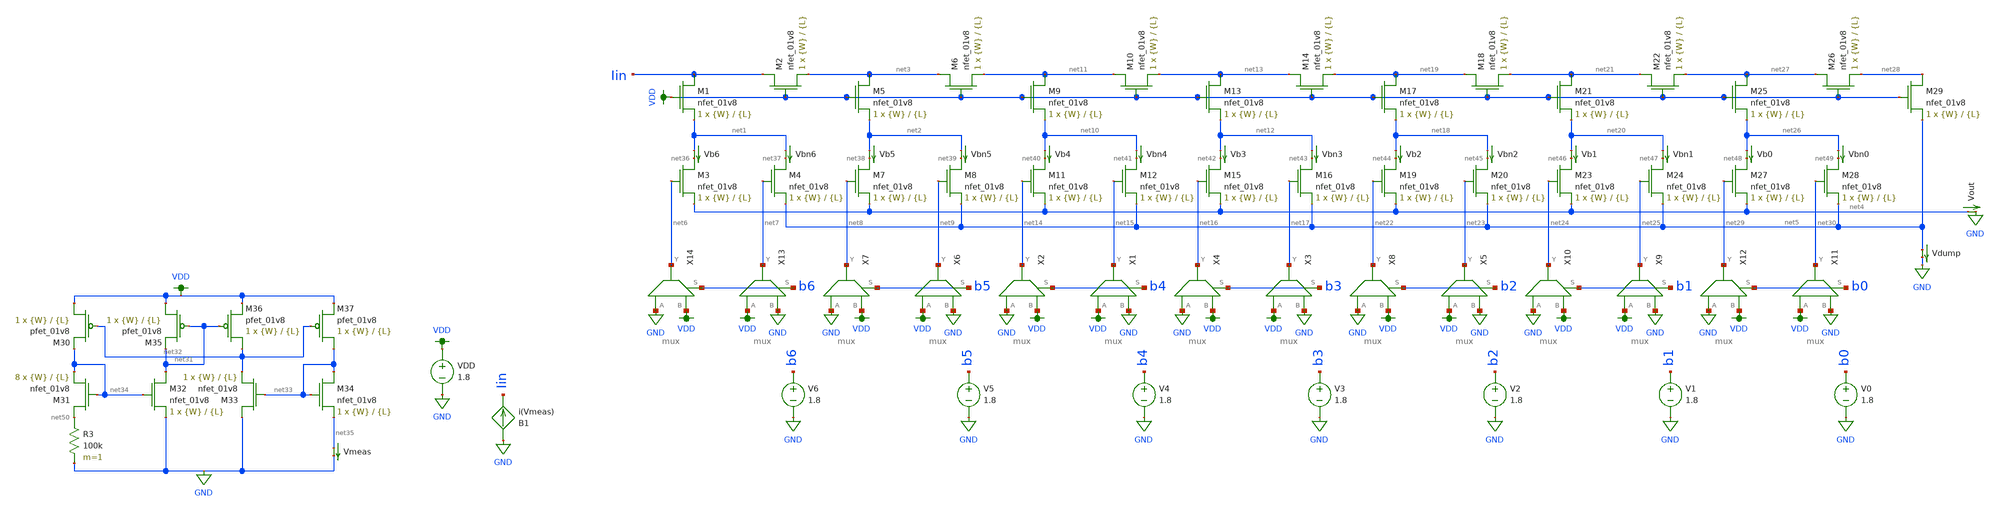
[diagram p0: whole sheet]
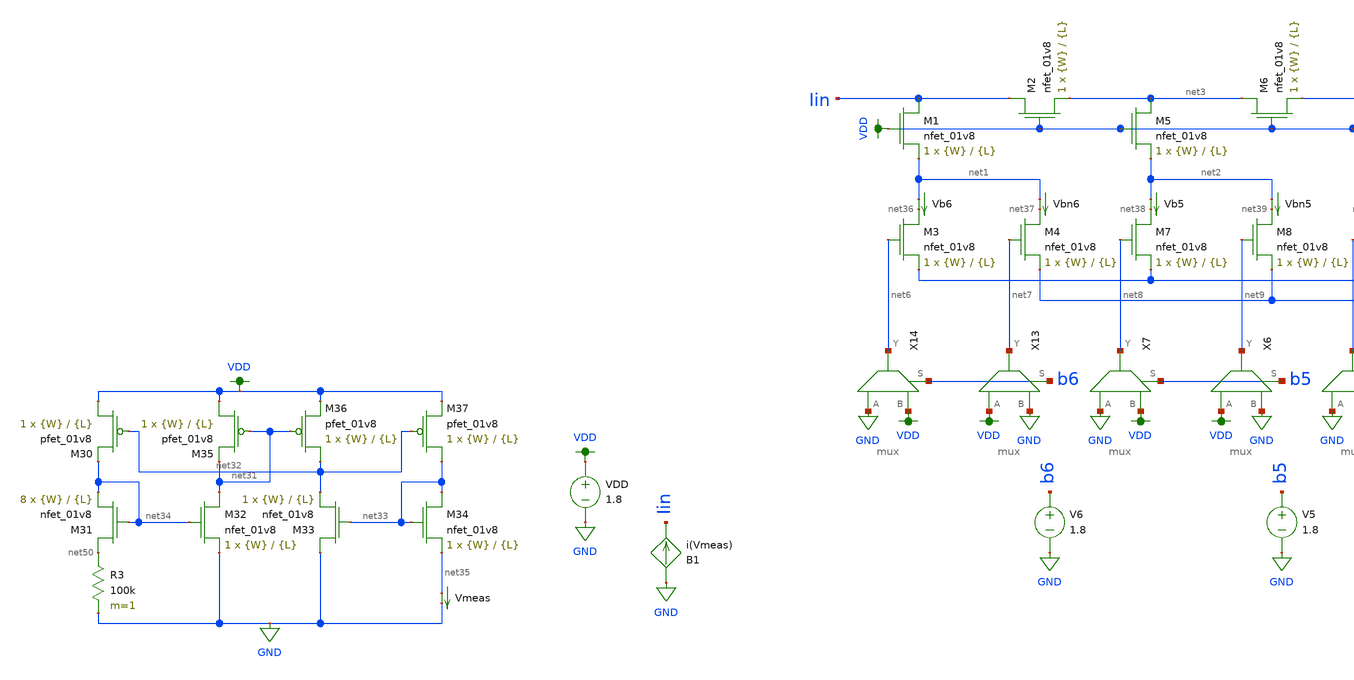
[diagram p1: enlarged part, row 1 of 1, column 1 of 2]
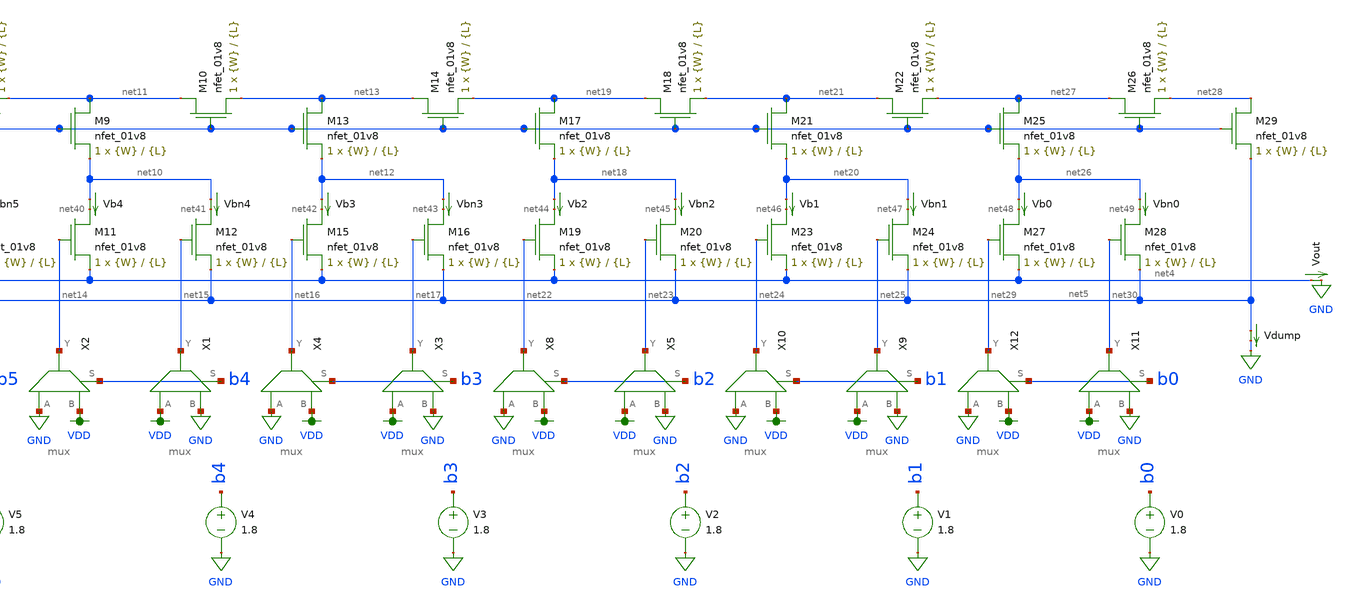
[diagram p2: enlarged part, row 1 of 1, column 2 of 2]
** sch_path: schematics/dac_from_paper.sch
**.subckt dac_from_paper
XM1 Iin VDD net1 GND sky130_fd_pr__nfet_01v8 L={L} W={W} nf=1 ad='int((nf+1)/2) * W/nf * 0.29' as='int((nf+2)/2) * W/nf * 0.29'
+ pd='2*int((nf+1)/2) * (W/nf + 0.29)' ps='2*int((nf+2)/2) * (W/nf + 0.29)' nrd='0.29 / W' nrs='0.29 / W'
+ sa=0 sb=0 sd=0 mult=1 m=1
XM2 Iin VDD net3 GND sky130_fd_pr__nfet_01v8 L={L} W={W} nf=1 ad='int((nf+1)/2) * W/nf * 0.29' as='int((nf+2)/2) * W/nf * 0.29'
+ pd='2*int((nf+1)/2) * (W/nf + 0.29)' ps='2*int((nf+2)/2) * (W/nf + 0.29)' nrd='0.29 / W' nrs='0.29 / W'
+ sa=0 sb=0 sd=0 mult=1 m=1
XM3 net36 net6 net4 GND sky130_fd_pr__nfet_01v8 L={L} W={W} nf=1 ad='int((nf+1)/2) * W/nf * 0.29' as='int((nf+2)/2) * W/nf * 0.29'
+ pd='2*int((nf+1)/2) * (W/nf + 0.29)' ps='2*int((nf+2)/2) * (W/nf + 0.29)' nrd='0.29 / W' nrs='0.29 / W'
+ sa=0 sb=0 sd=0 mult=1 m=1
XM4 net37 net7 net5 GND sky130_fd_pr__nfet_01v8 L={L} W={W} nf=1 ad='int((nf+1)/2) * W/nf * 0.29' as='int((nf+2)/2) * W/nf * 0.29'
+ pd='2*int((nf+1)/2) * (W/nf + 0.29)' ps='2*int((nf+2)/2) * (W/nf + 0.29)' nrd='0.29 / W' nrs='0.29 / W'
+ sa=0 sb=0 sd=0 mult=1 m=1
XM5 net3 VDD net2 GND sky130_fd_pr__nfet_01v8 L={L} W={W} nf=1 ad='int((nf+1)/2) * W/nf * 0.29' as='int((nf+2)/2) * W/nf * 0.29'
+ pd='2*int((nf+1)/2) * (W/nf + 0.29)' ps='2*int((nf+2)/2) * (W/nf + 0.29)' nrd='0.29 / W' nrs='0.29 / W'
+ sa=0 sb=0 sd=0 mult=1 m=1
XM6 net3 VDD net11 GND sky130_fd_pr__nfet_01v8 L={L} W={W} nf=1 ad='int((nf+1)/2) * W/nf * 0.29' as='int((nf+2)/2) * W/nf * 0.29'
+ pd='2*int((nf+1)/2) * (W/nf + 0.29)' ps='2*int((nf+2)/2) * (W/nf + 0.29)' nrd='0.29 / W' nrs='0.29 / W'
+ sa=0 sb=0 sd=0 mult=1 m=1
XM7 net38 net8 net4 GND sky130_fd_pr__nfet_01v8 L={L} W={W} nf=1 ad='int((nf+1)/2) * W/nf * 0.29' as='int((nf+2)/2) * W/nf * 0.29'
+ pd='2*int((nf+1)/2) * (W/nf + 0.29)' ps='2*int((nf+2)/2) * (W/nf + 0.29)' nrd='0.29 / W' nrs='0.29 / W'
+ sa=0 sb=0 sd=0 mult=1 m=1
XM8 net39 net9 net5 GND sky130_fd_pr__nfet_01v8 L={L} W={W} nf=1 ad='int((nf+1)/2) * W/nf * 0.29' as='int((nf+2)/2) * W/nf * 0.29'
+ pd='2*int((nf+1)/2) * (W/nf + 0.29)' ps='2*int((nf+2)/2) * (W/nf + 0.29)' nrd='0.29 / W' nrs='0.29 / W'
+ sa=0 sb=0 sd=0 mult=1 m=1
XM9 net11 VDD net10 GND sky130_fd_pr__nfet_01v8 L={L} W={W} nf=1 ad='int((nf+1)/2) * W/nf * 0.29' as='int((nf+2)/2) * W/nf * 0.29'
+ pd='2*int((nf+1)/2) * (W/nf + 0.29)' ps='2*int((nf+2)/2) * (W/nf + 0.29)' nrd='0.29 / W' nrs='0.29 / W'
+ sa=0 sb=0 sd=0 mult=1 m=1
XM10 net11 VDD net13 GND sky130_fd_pr__nfet_01v8 L={L} W={W} nf=1 ad='int((nf+1)/2) * W/nf * 0.29' as='int((nf+2)/2) * W/nf * 0.29'
+ pd='2*int((nf+1)/2) * (W/nf + 0.29)' ps='2*int((nf+2)/2) * (W/nf + 0.29)' nrd='0.29 / W' nrs='0.29 / W'
+ sa=0 sb=0 sd=0 mult=1 m=1
XM11 net40 net14 net4 GND sky130_fd_pr__nfet_01v8 L={L} W={W} nf=1 ad='int((nf+1)/2) * W/nf * 0.29' as='int((nf+2)/2) * W/nf * 0.29'
+ pd='2*int((nf+1)/2) * (W/nf + 0.29)' ps='2*int((nf+2)/2) * (W/nf + 0.29)' nrd='0.29 / W' nrs='0.29 / W'
+ sa=0 sb=0 sd=0 mult=1 m=1
XM12 net41 net15 net5 GND sky130_fd_pr__nfet_01v8 L={L} W={W} nf=1 ad='int((nf+1)/2) * W/nf * 0.29' as='int((nf+2)/2) * W/nf * 0.29'
+ pd='2*int((nf+1)/2) * (W/nf + 0.29)' ps='2*int((nf+2)/2) * (W/nf + 0.29)' nrd='0.29 / W' nrs='0.29 / W'
+ sa=0 sb=0 sd=0 mult=1 m=1
XM13 net13 VDD net12 GND sky130_fd_pr__nfet_01v8 L={L} W={W} nf=1 ad='int((nf+1)/2) * W/nf * 0.29' as='int((nf+2)/2) * W/nf * 0.29'
+ pd='2*int((nf+1)/2) * (W/nf + 0.29)' ps='2*int((nf+2)/2) * (W/nf + 0.29)' nrd='0.29 / W' nrs='0.29 / W'
+ sa=0 sb=0 sd=0 mult=1 m=1
XM14 net13 VDD net19 GND sky130_fd_pr__nfet_01v8 L={L} W={W} nf=1 ad='int((nf+1)/2) * W/nf * 0.29' as='int((nf+2)/2) * W/nf * 0.29'
+ pd='2*int((nf+1)/2) * (W/nf + 0.29)' ps='2*int((nf+2)/2) * (W/nf + 0.29)' nrd='0.29 / W' nrs='0.29 / W'
+ sa=0 sb=0 sd=0 mult=1 m=1
XM15 net42 net16 net4 GND sky130_fd_pr__nfet_01v8 L={L} W={W} nf=1 ad='int((nf+1)/2) * W/nf * 0.29' as='int((nf+2)/2) * W/nf * 0.29'
+ pd='2*int((nf+1)/2) * (W/nf + 0.29)' ps='2*int((nf+2)/2) * (W/nf + 0.29)' nrd='0.29 / W' nrs='0.29 / W'
+ sa=0 sb=0 sd=0 mult=1 m=1
XM16 net43 net17 net5 GND sky130_fd_pr__nfet_01v8 L={L} W={W} nf=1 ad='int((nf+1)/2) * W/nf * 0.29' as='int((nf+2)/2) * W/nf * 0.29'
+ pd='2*int((nf+1)/2) * (W/nf + 0.29)' ps='2*int((nf+2)/2) * (W/nf + 0.29)' nrd='0.29 / W' nrs='0.29 / W'
+ sa=0 sb=0 sd=0 mult=1 m=1
XM17 net19 VDD net18 GND sky130_fd_pr__nfet_01v8 L={L} W={W} nf=1 ad='int((nf+1)/2) * W/nf * 0.29' as='int((nf+2)/2) * W/nf * 0.29'
+ pd='2*int((nf+1)/2) * (W/nf + 0.29)' ps='2*int((nf+2)/2) * (W/nf + 0.29)' nrd='0.29 / W' nrs='0.29 / W'
+ sa=0 sb=0 sd=0 mult=1 m=1
XM18 net19 VDD net21 GND sky130_fd_pr__nfet_01v8 L={L} W={W} nf=1 ad='int((nf+1)/2) * W/nf * 0.29' as='int((nf+2)/2) * W/nf * 0.29'
+ pd='2*int((nf+1)/2) * (W/nf + 0.29)' ps='2*int((nf+2)/2) * (W/nf + 0.29)' nrd='0.29 / W' nrs='0.29 / W'
+ sa=0 sb=0 sd=0 mult=1 m=1
XM19 net44 net22 net4 GND sky130_fd_pr__nfet_01v8 L={L} W={W} nf=1 ad='int((nf+1)/2) * W/nf * 0.29' as='int((nf+2)/2) * W/nf * 0.29'
+ pd='2*int((nf+1)/2) * (W/nf + 0.29)' ps='2*int((nf+2)/2) * (W/nf + 0.29)' nrd='0.29 / W' nrs='0.29 / W'
+ sa=0 sb=0 sd=0 mult=1 m=1
XM20 net45 net23 net5 GND sky130_fd_pr__nfet_01v8 L={L} W={W} nf=1 ad='int((nf+1)/2) * W/nf * 0.29' as='int((nf+2)/2) * W/nf * 0.29'
+ pd='2*int((nf+1)/2) * (W/nf + 0.29)' ps='2*int((nf+2)/2) * (W/nf + 0.29)' nrd='0.29 / W' nrs='0.29 / W'
+ sa=0 sb=0 sd=0 mult=1 m=1
XM21 net21 VDD net20 GND sky130_fd_pr__nfet_01v8 L={L} W={W} nf=1 ad='int((nf+1)/2) * W/nf * 0.29' as='int((nf+2)/2) * W/nf * 0.29'
+ pd='2*int((nf+1)/2) * (W/nf + 0.29)' ps='2*int((nf+2)/2) * (W/nf + 0.29)' nrd='0.29 / W' nrs='0.29 / W'
+ sa=0 sb=0 sd=0 mult=1 m=1
XM22 net21 VDD net27 GND sky130_fd_pr__nfet_01v8 L={L} W={W} nf=1 ad='int((nf+1)/2) * W/nf * 0.29' as='int((nf+2)/2) * W/nf * 0.29'
+ pd='2*int((nf+1)/2) * (W/nf + 0.29)' ps='2*int((nf+2)/2) * (W/nf + 0.29)' nrd='0.29 / W' nrs='0.29 / W'
+ sa=0 sb=0 sd=0 mult=1 m=1
XM23 net46 net24 net4 GND sky130_fd_pr__nfet_01v8 L={L} W={W} nf=1 ad='int((nf+1)/2) * W/nf * 0.29' as='int((nf+2)/2) * W/nf * 0.29'
+ pd='2*int((nf+1)/2) * (W/nf + 0.29)' ps='2*int((nf+2)/2) * (W/nf + 0.29)' nrd='0.29 / W' nrs='0.29 / W'
+ sa=0 sb=0 sd=0 mult=1 m=1
XM24 net47 net25 net5 GND sky130_fd_pr__nfet_01v8 L={L} W={W} nf=1 ad='int((nf+1)/2) * W/nf * 0.29' as='int((nf+2)/2) * W/nf * 0.29'
+ pd='2*int((nf+1)/2) * (W/nf + 0.29)' ps='2*int((nf+2)/2) * (W/nf + 0.29)' nrd='0.29 / W' nrs='0.29 / W'
+ sa=0 sb=0 sd=0 mult=1 m=1
XM25 net27 VDD net26 GND sky130_fd_pr__nfet_01v8 L={L} W={W} nf=1 ad='int((nf+1)/2) * W/nf * 0.29' as='int((nf+2)/2) * W/nf * 0.29'
+ pd='2*int((nf+1)/2) * (W/nf + 0.29)' ps='2*int((nf+2)/2) * (W/nf + 0.29)' nrd='0.29 / W' nrs='0.29 / W'
+ sa=0 sb=0 sd=0 mult=1 m=1
XM26 net27 VDD net28 GND sky130_fd_pr__nfet_01v8 L={L} W={W} nf=1 ad='int((nf+1)/2) * W/nf * 0.29' as='int((nf+2)/2) * W/nf * 0.29'
+ pd='2*int((nf+1)/2) * (W/nf + 0.29)' ps='2*int((nf+2)/2) * (W/nf + 0.29)' nrd='0.29 / W' nrs='0.29 / W'
+ sa=0 sb=0 sd=0 mult=1 m=1
XM27 net48 net29 net4 GND sky130_fd_pr__nfet_01v8 L={L} W={W} nf=1 ad='int((nf+1)/2) * W/nf * 0.29' as='int((nf+2)/2) * W/nf * 0.29'
+ pd='2*int((nf+1)/2) * (W/nf + 0.29)' ps='2*int((nf+2)/2) * (W/nf + 0.29)' nrd='0.29 / W' nrs='0.29 / W'
+ sa=0 sb=0 sd=0 mult=1 m=1
XM28 net49 net30 net5 GND sky130_fd_pr__nfet_01v8 L={L} W={W} nf=1 ad='int((nf+1)/2) * W/nf * 0.29' as='int((nf+2)/2) * W/nf * 0.29'
+ pd='2*int((nf+1)/2) * (W/nf + 0.29)' ps='2*int((nf+2)/2) * (W/nf + 0.29)' nrd='0.29 / W' nrs='0.29 / W'
+ sa=0 sb=0 sd=0 mult=1 m=1
XM29 net28 VDD net5 GND sky130_fd_pr__nfet_01v8 L={L} W={W} nf=1 ad='int((nf+1)/2) * W/nf * 0.29' as='int((nf+2)/2) * W/nf * 0.29'
+ pd='2*int((nf+1)/2) * (W/nf + 0.29)' ps='2*int((nf+2)/2) * (W/nf + 0.29)' nrd='0.29 / W' nrs='0.29 / W'
+ sa=0 sb=0 sd=0 mult=1 m=1
Vdump net5 GND 0
.save i(vdump)
Vb0 net26 net48 0
.save i(vb0)
Vbn0 net26 net49 0
.save i(vbn0)
Vb5 net2 net38 0
.save i(vb5)
Vb6 net1 net36 0
.save i(vb6)
Vout net4 GND 0
.save i(vout)
Vb1 net20 net46 0
.save i(vb1)
Vb2 net18 net44 0
.save i(vb2)
Vb3 net12 net42 0
.save i(vb3)
Vb4 net10 net40 0
.save i(vb4)
Vbn1 net20 net47 0
.save i(vbn1)
Vbn2 net18 net45 0
.save i(vbn2)
Vbn3 net12 net43 0
.save i(vbn3)
Vbn4 net10 net41 0
.save i(vbn4)
Vbn5 net2 net39 0
.save i(vbn5)
Vbn6 net1 net37 0
.save i(vbn6)
V0 b0 GND 1.8
V1 b1 GND 1.8
V2 b2 GND 1.8
V3 b3 GND 1.8
V4 b4 GND 1.8
V5 b5 GND 1.8
V6 b6 GND 1.8
XM30 VDD net32 net34 VDD sky130_fd_pr__pfet_01v8 L={L} W={W} nf=1 ad='int((nf+1)/2) * W/nf * 0.29' as='int((nf+2)/2) * W/nf * 0.29'
+ pd='2*int((nf+1)/2) * (W/nf + 0.29)' ps='2*int((nf+2)/2) * (W/nf + 0.29)' nrd='0.29 / W' nrs='0.29 / W'
+ sa=0 sb=0 sd=0 mult=1 m=1
XM31 net50 net34 net34 GND sky130_fd_pr__nfet_01v8 L={L} W={W} nf=1 ad='int((nf+1)/2) * W/nf * 0.29'
+ as='int((nf+2)/2) * W/nf * 0.29' pd='2*int((nf+1)/2) * (W/nf + 0.29)' ps='2*int((nf+2)/2) * (W/nf + 0.29)'
+ nrd='0.29 / W' nrs='0.29 / W' sa=0 sb=0 sd=0 mult=8 m=8
R3 net50 GND 100k m=1
XM32 net31 net34 GND GND sky130_fd_pr__nfet_01v8 L={L} W={W} nf=1 ad='int((nf+1)/2) * W/nf * 0.29' as='int((nf+2)/2) * W/nf * 0.29'
+ pd='2*int((nf+1)/2) * (W/nf + 0.29)' ps='2*int((nf+2)/2) * (W/nf + 0.29)' nrd='0.29 / W' nrs='0.29 / W'
+ sa=0 sb=0 sd=0 mult=1 m=1
XM33 GND net33 net32 GND sky130_fd_pr__nfet_01v8 L={L} W={W} nf=1 ad='int((nf+1)/2) * W/nf * 0.29' as='int((nf+2)/2) * W/nf * 0.29'
+ pd='2*int((nf+1)/2) * (W/nf + 0.29)' ps='2*int((nf+2)/2) * (W/nf + 0.29)' nrd='0.29 / W' nrs='0.29 / W'
+ sa=0 sb=0 sd=0 mult=1 m=1
XM34 net33 net33 net35 GND sky130_fd_pr__nfet_01v8 L={L} W={W} nf=1 ad='int((nf+1)/2) * W/nf * 0.29'
+ as='int((nf+2)/2) * W/nf * 0.29' pd='2*int((nf+1)/2) * (W/nf + 0.29)' ps='2*int((nf+2)/2) * (W/nf + 0.29)'
+ nrd='0.29 / W' nrs='0.29 / W' sa=0 sb=0 sd=0 mult=1 m=1
XM35 VDD net31 net31 VDD sky130_fd_pr__pfet_01v8 L={L} W={W} nf=1 ad='int((nf+1)/2) * W/nf * 0.29' as='int((nf+2)/2) * W/nf * 0.29'
+ pd='2*int((nf+1)/2) * (W/nf + 0.29)' ps='2*int((nf+2)/2) * (W/nf + 0.29)' nrd='0.29 / W' nrs='0.29 / W'
+ sa=0 sb=0 sd=0 mult=1 m=1
XM36 net32 net31 VDD VDD sky130_fd_pr__pfet_01v8 L={L} W={W} nf=1 ad='int((nf+1)/2) * W/nf * 0.29' as='int((nf+2)/2) * W/nf * 0.29'
+ pd='2*int((nf+1)/2) * (W/nf + 0.29)' ps='2*int((nf+2)/2) * (W/nf + 0.29)' nrd='0.29 / W' nrs='0.29 / W'
+ sa=0 sb=0 sd=0 mult=1 m=1
XM37 net33 net32 VDD VDD sky130_fd_pr__pfet_01v8 L={L} W={W} nf=1 ad='int((nf+1)/2) * W/nf * 0.29' as='int((nf+2)/2) * W/nf * 0.29'
+ pd='2*int((nf+1)/2) * (W/nf + 0.29)' ps='2*int((nf+2)/2) * (W/nf + 0.29)' nrd='0.29 / W' nrs='0.29 / W'
+ sa=0 sb=0 sd=0 mult=1 m=1
VDD VDD GND 1.8
Vmeas net35 GND 0
.save i(vmeas)
B1 GND Iin I=i(Vmeas)
X13 VDD GND net7 b6 mux
X14 GND VDD net6 b6 mux
X6 VDD GND net9 b5 mux
X7 GND VDD net8 b5 mux
X1 VDD GND net15 b4 mux
X2 GND VDD net14 b4 mux
X3 VDD GND net17 b3 mux
X4 GND VDD net16 b3 mux
X5 VDD GND net23 b2 mux
X8 GND VDD net22 b2 mux
X9 VDD GND net25 b1 mux
X10 GND VDD net24 b1 mux
X11 VDD GND net30 b0 mux
X12 GND VDD net29 b0 mux
**** begin user architecture code

.option wnflag=1
.param MC_SWITCH=1.0
.lib ~/skywater/skywater-pdk/libraries/sky130_fd_pr_ngspice/latest/models/sky130.lib.spice tt


.param W=32
.param L=4
.control
set wr_vecnames
set wr_singlescale
let code = 0
  while code < 128
    if code eq 0
      let b0 = 0
    else
      let b0 = code % 2
    end
    if floor(code / 2) eq 0
      let b1 = 0
    else
      let b1 = floor(code / 2) % 2
    end
    if floor(code / 4) eq 0
      let b2 = 0
    else
      let b2 = floor(code / 4) % 2
    end
    if floor(code / 8) eq 0
      let b3 = 0
    else
      let b3 = floor(code / 8) % 2
    end
    if floor(code / 16) eq 0
      let b4 = 0
    else
      let b4 = floor(code / 16) % 2
    end
    if floor(code / 32) eq 0
      let b5 = 0
    else
      let b5 = floor(code / 32) % 2
    end
    if floor(code / 64) eq 0
      let b6 = 0
    else
      let b6 = floor(code / 64) % 2
    end
    alter v0 $&b0
    alter v1 $&b1
    alter v2 $&b2
    alter v3 $&b3
    alter v4 $&b4
    alter v5 $&b5
    alter v6 $&b6
    save all
    op
    wrdata ~/Documents/current-output-dac-vlsi/simulations/dac_paper_sim.txt i(Vmeas) i(vb0) i(vb1)
+ i(vb2) i(vb3) i(vb4) i(vb5) i(vb6) i(Vout) i(Vdump)
    if code eq 0
      set appendwrite
      set wr_vecnames = FALSE
    end
    let code = code + 1
  end
  quit
.endc

**** end user architecture code
**.ends

* expanding   symbol:  /home/madvlsi/Documents/current-output-dac-vlsi/schematics/mux.sym # of
*+ pins=4
** sym_path: /home/madvlsi/Documents/current-output-dac-vlsi/schematics/mux.sym
** sch_path: /home/madvlsi/Documents/current-output-dac-vlsi/schematics/mux.sch
.subckt mux A B Y S
*.ipin S
*.ipin A
*.opin Y
*.ipin B
XM1 net1 S GND GND sky130_fd_pr__nfet_01v8 L=0.15 W=1 nf=1 ad='int((nf+1)/2) * W/nf * 0.29' as='int((nf+2)/2) * W/nf * 0.29'
+ pd='2*int((nf+1)/2) * (W/nf + 0.29)' ps='2*int((nf+2)/2) * (W/nf + 0.29)' nrd='0.29 / W' nrs='0.29 / W'
+ sa=0 sb=0 sd=0 mult=1 m=1
XM2 net1 S VDD VDD sky130_fd_pr__pfet_01v8 L=0.15 W=1 nf=1 ad='int((nf+1)/2) * W/nf * 0.29' as='int((nf+2)/2) * W/nf * 0.29'
+ pd='2*int((nf+1)/2) * (W/nf + 0.29)' ps='2*int((nf+2)/2) * (W/nf + 0.29)' nrd='0.29 / W' nrs='0.29 / W'
+ sa=0 sb=0 sd=0 mult=1 m=1
XM3 Y S B GND sky130_fd_pr__nfet_01v8 L=0.15 W=1 nf=1 ad='int((nf+1)/2) * W/nf * 0.29' as='int((nf+2)/2) * W/nf * 0.29'
+ pd='2*int((nf+1)/2) * (W/nf + 0.29)' ps='2*int((nf+2)/2) * (W/nf + 0.29)' nrd='0.29 / W' nrs='0.29 / W'
+ sa=0 sb=0 sd=0 mult=1 m=1
XM4 A net1 Y GND sky130_fd_pr__nfet_01v8 L=0.15 W=1 nf=1 ad='int((nf+1)/2) * W/nf * 0.29' as='int((nf+2)/2) * W/nf * 0.29'
+ pd='2*int((nf+1)/2) * (W/nf + 0.29)' ps='2*int((nf+2)/2) * (W/nf + 0.29)' nrd='0.29 / W' nrs='0.29 / W'
+ sa=0 sb=0 sd=0 mult=1 m=1
.ends

.GLOBAL GND
.GLOBAL VDD
.end
